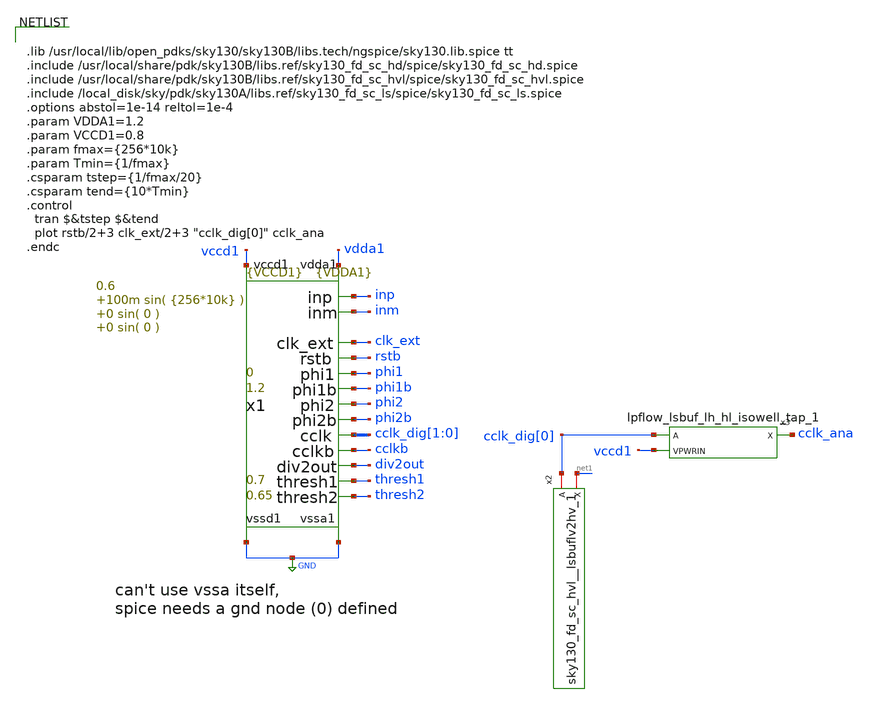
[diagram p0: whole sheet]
** sch_path: xschem/test_bench/sky130_hvl_level_shifter_tb.sch
**.subckt sky130_hvl_level_shifter_tb
x1 thresh1 thresh2 vdda1 GND inp inm clk_ext rstb vccd1 GND phi1 phi1b phi2 phi2b cclk_dig[1] cclkb div2out
+ risc_signals p_vdda1={VDDA1} p_vccd1={VCCD1} p_fclk={256*10k} p_duty_cycle=0.5 p_rstb_delay={1.5/p_fclk}
+ p_rstb_tr=5n p_thresh1=0.7 p_thresh2=0.65 p_vpb=0 p_vnb=1.2 p_vcm=0.6 p_amp1=100m p_f1={256*10k} p_amp2=0
+ p_f2=0 p_amp3=0 p_f3=0
x2 cclk_dig[0] vccd1 GND GND vdda1 vdda1 net1 sky130_fd_sc_hvl__lsbuflv2hv_1
x3 cclk_dig[0] GND vdda1 vccd1 vdda1 cclk_ana sky130_fd_sc_hd__lpflow_lsbuf_lh_hl_isowell_tap_1
**** begin user architecture code


.lib /usr/local/lib/open_pdks/sky130/sky130B/libs.tech/ngspice/sky130.lib.spice tt
.include /usr/local/share/pdk/sky130B/libs.ref/sky130_fd_sc_hd/spice/sky130_fd_sc_hd.spice
.include /usr/local/share/pdk/sky130B/libs.ref/sky130_fd_sc_hvl/spice/sky130_fd_sc_hvl.spice
.include /local_disk/sky/pdk/sky130A/libs.ref/sky130_fd_sc_ls/spice/sky130_fd_sc_ls.spice
.options abstol=1e-14 reltol=1e-4
.param VDDA1=1.2
.param VCCD1=0.8
.param fmax={256*10k}
.param Tmin={1/fmax}
.csparam tstep={1/fmax/20}
.csparam tend={10*Tmin}
.control
  tran $&tstep $&tend
  plot rstb/2+3 clk_ext/2+3 "cclk_dig[0]" cclk_ana
.endc


**** end user architecture code
**.ends
.GLOBAL GND
.end
